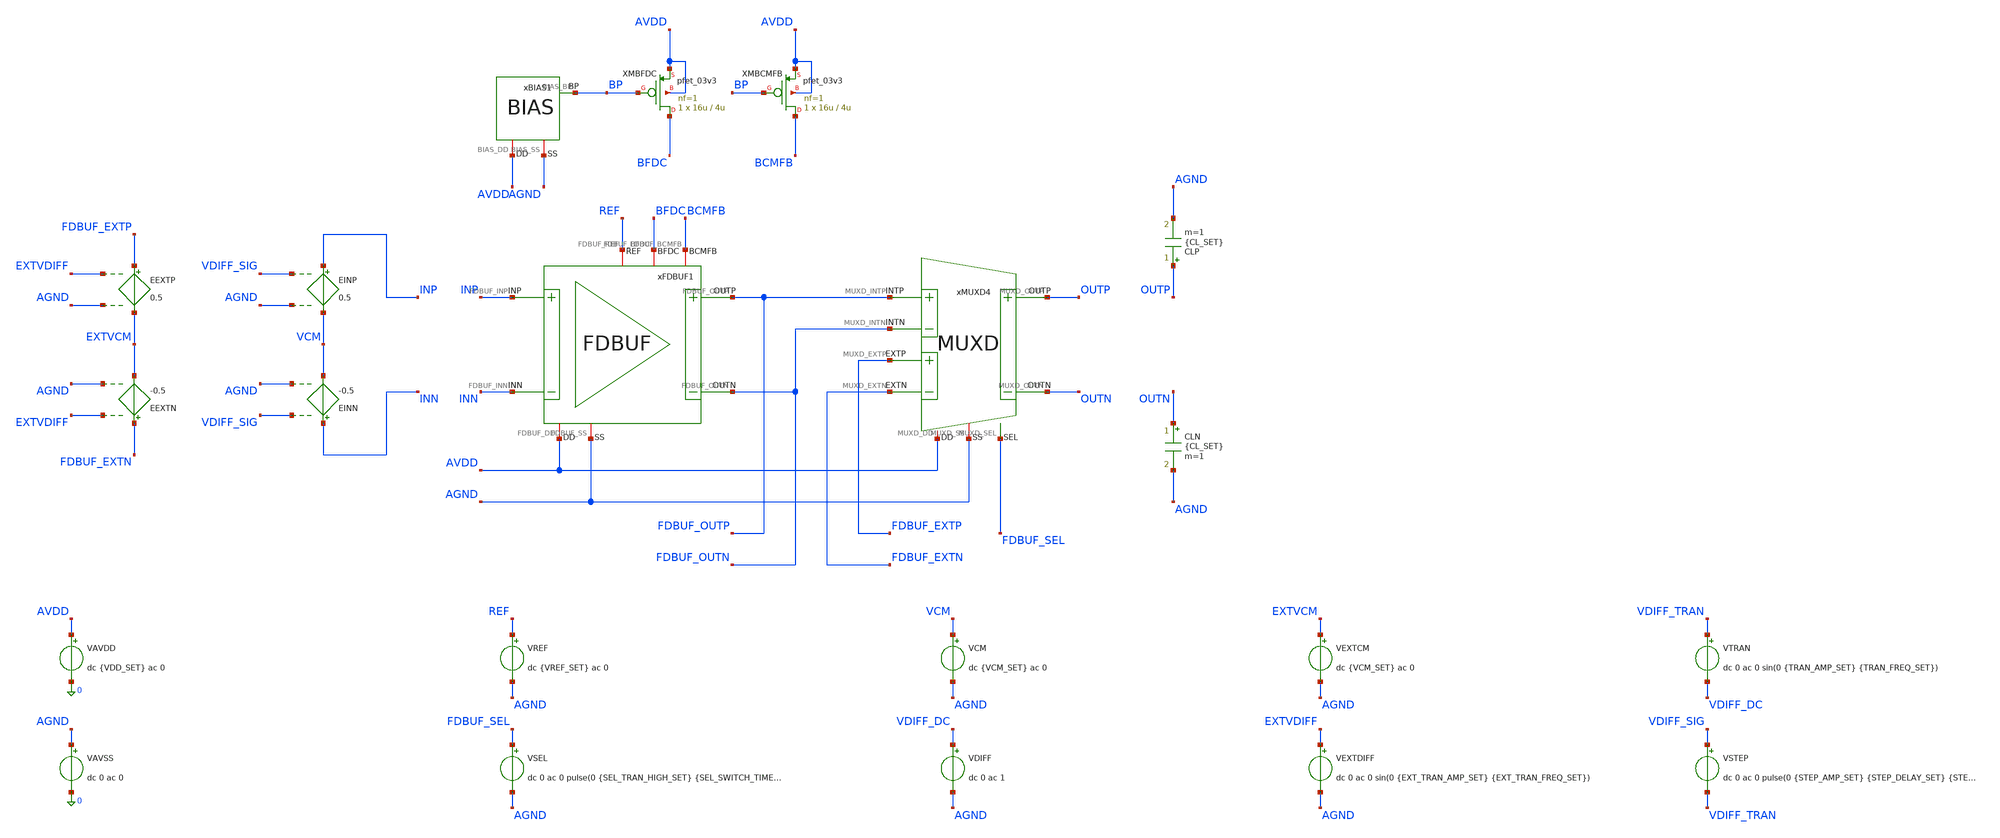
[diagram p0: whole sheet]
** sch_path: Design_Files/IC Design/Testbench/AFE_BLOCKS/FDBUF/FDBUF_TB_MC.sch
**.subckt FDBUF_TB_MC
CLP OUTP AGND {CL_SET} m=1
CLN OUTN AGND {CL_SET} m=1
xBIAS1 AVDD AGND BP BIAS
XMBFDC BFDC BP AVDD AVDD pfet_03v3 L=4u W=16u nf=1 ad='int((nf+1)/2) * W/nf * 0.18u' as='int((nf+2)/2) * W/nf * 0.18u'
+ pd='2*int((nf+1)/2) * (W/nf + 0.18u)' ps='2*int((nf+2)/2) * (W/nf + 0.18u)' nrd='0.18u / W' nrs='0.18u / W'
+ sa=0 sb=0 sd=0 m=1
XMBCMFB BCMFB BP AVDD AVDD pfet_03v3 L=4u W=16u nf=1 ad='int((nf+1)/2) * W/nf * 0.18u' as='int((nf+2)/2) * W/nf * 0.18u'
+ pd='2*int((nf+1)/2) * (W/nf + 0.18u)' ps='2*int((nf+2)/2) * (W/nf + 0.18u)' nrd='0.18u / W' nrs='0.18u / W'
+ sa=0 sb=0 sd=0 m=1
VAVDD AVDD 0 dc {VDD_SET} ac 0
.save i(vavdd)
VAVSS AGND 0 dc 0 ac 0
xFDBUF1 AVDD AGND INP INN FDBUF_OUTN BFDC FDBUF_OUTP BCMFB REF FDBUF
xMUXD4 AVDD AGND FDBUF_OUTP FDBUF_OUTN OUTN OUTP FDBUF_EXTP FDBUF_EXTN FDBUF_SEL MUXD
VCM VCM AGND dc {VCM_SET} ac 0
VDIFF VDIFF_DC AGND dc 0 ac 1
VREF REF AGND dc {VREF_SET} ac 0
VSEL FDBUF_SEL AGND dc 0 ac 0 pulse(0 {SEL_TRAN_HIGH_SET} {SEL_SWITCH_TIME_SET} 1u 1u 400m 800m)
VEXTCM EXTVCM AGND dc {VCM_SET} ac 0
VEXTDIFF EXTVDIFF AGND dc 0 ac 0 sin(0 {EXT_TRAN_AMP_SET} {EXT_TRAN_FREQ_SET})
EINP INP VCM VDIFF_SIG AGND 0.5
EINN INN VCM VDIFF_SIG AGND -0.5
EEXTP FDBUF_EXTP EXTVCM EXTVDIFF AGND 0.5
EEXTN FDBUF_EXTN EXTVCM EXTVDIFF AGND -0.5
VTRAN VDIFF_TRAN VDIFF_DC dc 0 ac 0 sin(0 {TRAN_AMP_SET} {TRAN_FREQ_SET})
VSTEP VDIFF_SIG VDIFF_TRAN dc 0 ac 0 pulse(0 {STEP_AMP_SET} {STEP_DELAY_SET} {STEP_TR_SET} {STEP_TF_SET}
+ {STEP_PW_SET} {STEP_PERIOD_SET})
**** begin user architecture code

* {MODELS_START}
.include $::180MCU_MODELS/design.ngspice

.param sw_stat_global=0
.param sw_stat_mismatch=1

.param mc_skew=3
.param res_mc_skew=3
.param cap_mc_skew=3

.lib $::180MCU_MODELS/sm141064.ngspice statistical
.lib $::180MCU_MODELS/sm141064.ngspice res_statistical
.lib $::180MCU_MODELS/sm141064.ngspice mimcap_statistical
.lib $::180MCU_MODELS/sm141064.ngspice cap_mim
.lib $::180MCU_MODELS/sm141064.ngspice bjt_statistical
* {MODELS_END}



* {SETUP_START}
.param VDD_SET=3.3
.param TEMP_SET=27

.param VCM_SET={VDD_SET/2}
.param VREF_SET={VDD_SET/2}

.param CL_SET=60p

.param FDBUF_GAIN_TARGET_SET=1

.param TRAN_AMP_SET=0
.param TRAN_FREQ_SET=10

.param STEP_AMP_SET=0
.param STEP_DELAY_SET=20u
.param STEP_TR_SET=10n
.param STEP_TF_SET=10n
.param STEP_PW_SET=100u
.param STEP_PERIOD_SET=200u

.param EXT_TRAN_AMP_SET=0
.param EXT_TRAN_FREQ_SET=25

.param SEL_TRAN_HIGH_SET=0
.param SEL_SWITCH_TIME_SET=200m

.csparam MC_RUNS=200

.temp {TEMP_SET}

.options gmin=1e-12
.options rshunt=1e12
.options method=gear
* {SETUP_END}




* {MEAS_START}
.control

destroy all

set noaskquit
set wr_singlescale
unset wr_vecnames

option klu
option numdgt=15
option method=gear
option maxord=2
option plotwinsize=0

let mode_index=0

dowhile mode_index < 3

if mode_index = 0
set mode=mm
set tag=mm
alterparam sw_stat_global=0
alterparam sw_stat_mismatch=1
end

if mode_index = 1
set mode=gl
set tag=gl
alterparam sw_stat_global=1
alterparam sw_stat_mismatch=0
end

if mode_index = 2
set mode=full
set tag=full
alterparam sw_stat_global=1
alterparam sw_stat_mismatch=1
end

alterparam VDD_SET=3.3
alterparam TEMP_SET=27

alterparam TRAN_AMP_SET=0
alterparam STEP_AMP_SET=0
alterparam EXT_TRAN_AMP_SET=0
alterparam SEL_TRAN_HIGH_SET=0

reset

shell mkdir -p /foss/designs/ECG_Acquisition_IC/Measurement_Results/IC_Simulation/AFE_BLOCKS/FDBUF/{$mode}.Result_txt

shell rm -f /foss/designs/ECG_Acquisition_IC/Measurement_Results/IC_Simulation/AFE_BLOCKS/FDBUF/{$mode}.Result_txt/{$tag}.l40_mc_summary.txt
shell rm -f /foss/designs/ECG_Acquisition_IC/Measurement_Results/IC_Simulation/AFE_BLOCKS/FDBUF/{$mode}.Result_txt/{$tag}.l60_mc_summary.txt
shell rm -f /foss/designs/ECG_Acquisition_IC/Measurement_Results/IC_Simulation/AFE_BLOCKS/FDBUF/{$mode}.Result_txt/{$tag}.l80_mc_summary.txt
shell rm -f /foss/designs/ECG_Acquisition_IC/Measurement_Results/IC_Simulation/AFE_BLOCKS/FDBUF/{$mode}.Result_txt/{$tag}.l100_mc_summary.txt

let run=1

dowhile run <= $&MC_RUNS

setseed $&run
mc_source

save all
save @m.xmbfdc.m0[id]
save @m.xmbcmfb.m0[id]

* SOURCE STATE

alter @VAVDD[DC]=3.3
alter @VAVSS[DC]=0

alter @VCM[DC]=1.65
alter @VREF[DC]=1.65

alter @VSEL[DC]=0
alter @VDIFF[DC]=0

alter @VAVDD[ACMAG]=0
alter @VAVSS[ACMAG]=0
alter @VCM[ACMAG]=0
alter @VREF[ACMAG]=0
alter @VDIFF[ACMAG]=0
alter @VEXTDIFF[ACMAG]=0

alter CLP 60p
alter CLN 60p

* OFFSET
* shared by all loads

dc VDIFF -20m 20m 20u

let buffer_diff=v(FDBUF_OUTP)-v(FDBUF_OUTN)

meas dc vos_meas when buffer_diff=0 cross=1

set vos_val=$&vos_meas

destroy all

alter @VDIFF[DC]=$vos_val

* OP
* shared by all loads

op

let buffer_out_cm=0.5*(v(FDBUF_OUTP)+v(FDBUF_OUTN))-v(AGND)
let out_cm_error=buffer_out_cm-v(REF)

let idd_total=abs(vavdd#branch)
let power_total=(v(AVDD)-v(AGND))*idd_total

let ibfdc=abs(@m.xmbfdc.m0[id])
let ibcmfb=abs(@m.xmbcmfb.m0[id])

set idd_val=$&idd_total
set power_val=$&power_total
set outcmerr_val=$&out_cm_error
set ibfdc_val=$&ibfdc
set ibcmfb_val=$&ibcmfb

destroy all

* FOUR LOADS

foreach lcode 0 1 2 3

if $lcode = 0
set ltag=l40
set cload=40p
else
if $lcode = 1
set ltag=l60
set cload=60p
else
if $lcode = 2
set ltag=l80
set cload=80p
else
set ltag=l100
set cload=100p
end
end
end

alter CLP $cload
alter CLN $cload

alter @VDIFF[DC]=$vos_val

* DIFF AC

alter @VDIFF[ACMAG]=1
alter @VCM[ACMAG]=0
alter @VREF[ACMAG]=0
alter @VEXTDIFF[ACMAG]=0
alter @VAVDD[ACMAG]=0
alter @VAVSS[ACMAG]=0

ac dec 100 10 100Meg

let vin_diff=v(INP)-v(INN)
let buffer_diff=v(FDBUF_OUTP)-v(FDBUF_OUTN)

let buffer_gain=mag(buffer_diff/vin_diff)

meas ac gain10 find buffer_gain at=10

meas ac ad60 find buffer_gain at=60
meas ac ad150 find buffer_gain at=150

let norm_db=20*log10(buffer_gain/$&gain10)

meas ac bw3db when norm_db=-3 fall=1

let gain_error_pct=100*($&gain10/1-1)

set gain10_val=$&gain10
set gainerr_val=$&gain_error_pct
set bw3db_val=$&bw3db

set ad60_val=$&ad60
set ad150_val=$&ad150

destroy all

* CMRR

alter @VDIFF[ACMAG]=0
alter @VCM[ACMAG]=1
alter @VREF[ACMAG]=0
alter @VEXTDIFF[ACMAG]=0
alter @VAVDD[ACMAG]=0
alter @VAVSS[ACMAG]=0

ac lin 1 60 60

let vin_cm=0.5*(v(INP)+v(INN))-v(AGND)
let buffer_diff=v(FDBUF_OUTP)-v(FDBUF_OUTN)

let acm60=mag(buffer_diff/vin_cm)

set acm60_val=$&acm60

destroy all

ac lin 1 150 150

let vin_cm=0.5*(v(INP)+v(INN))-v(AGND)
let buffer_diff=v(FDBUF_OUTP)-v(FDBUF_OUTN)
let acm150=mag(buffer_diff/vin_cm)

set acm150_val=$&acm150

let cmrr60=20*log10($ad60_val/$acm60_val)
let cmrr150=20*log10($ad150_val/$acm150_val)

set cmrr60_val=$&cmrr60
set cmrr150_val=$&cmrr150

destroy all

* SUMMARY

echo $&run $ibfdc_val $ibcmfb_val $idd_val $power_val $outcmerr_val $vos_val $gain10_val $gainerr_val
+ $bw3db_val $cmrr60_val $cmrr150_val >> /foss/designs/ECG_Acquisition_IC/Measurement_Results/IC_Simulation/AFE_BLOCKS/FDBUF/{$mode}.Result_txt/{$tag}.{$ltag}_mc_summary.txt

end

let run=run+1

end

let mode_index=mode_index+1

end

quit

.endc
* {MEAS_END}


**** end user architecture code
**.ends
.end
